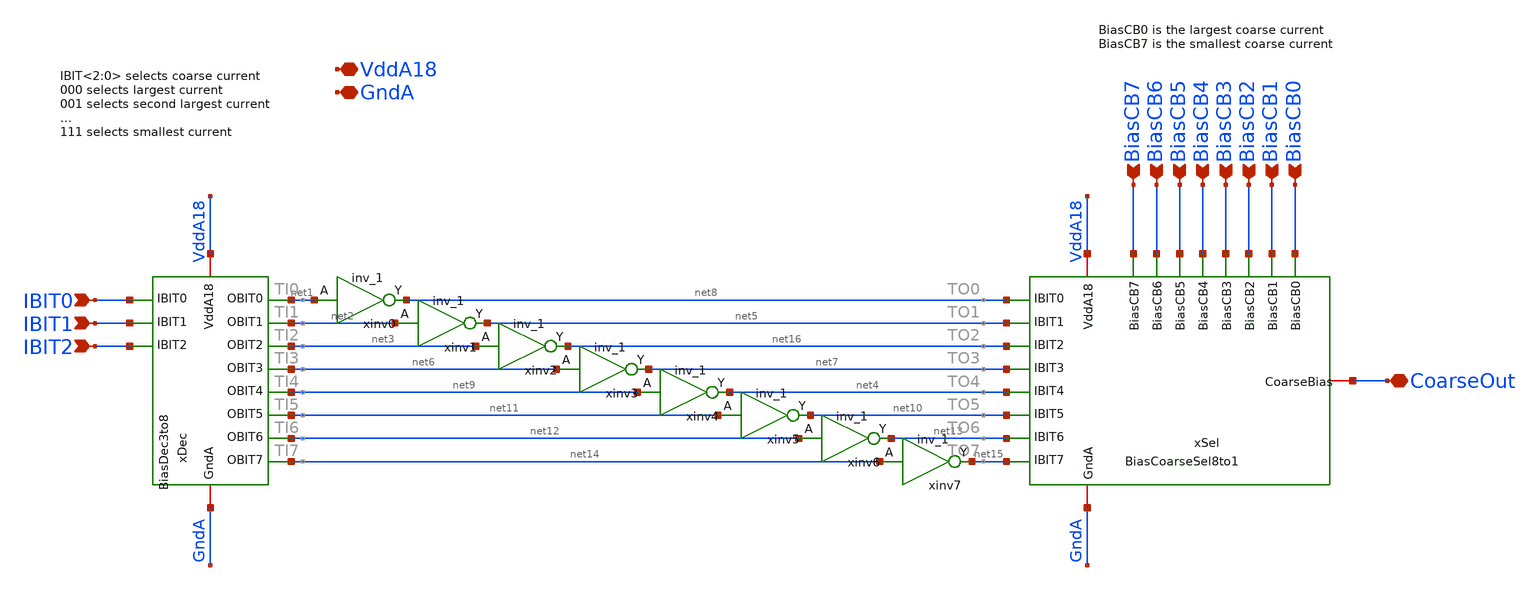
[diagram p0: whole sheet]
** sch_path: analog/xschem/BiasCoarseBuffer.sch
**.subckt BiasCoarseBuffer VddA18 GndA BiasCB7 BiasCB6 BiasCB5 BiasCB4 BiasCB3 BiasCB2 BiasCB1
*+ BiasCB0 IBIT0 IBIT1 IBIT2 CoarseOut
*.iopin VddA18
*.iopin GndA
*.ipin BiasCB7
*.ipin BiasCB6
*.ipin BiasCB5
*.ipin BiasCB4
*.ipin BiasCB3
*.ipin BiasCB2
*.ipin BiasCB1
*.ipin BiasCB0
*.ipin IBIT0
*.ipin IBIT1
*.ipin IBIT2
*.iopin CoarseOut
xSel VddA18 GndA net8 net5 net7 net4 net10 net13 net15 net16 BiasCB0 BiasCB1 BiasCB3 BiasCB4 BiasCB5
+ BiasCB6 BiasCB7 BiasCB2 CoarseOut BiasCoarseSel8to1
xDec VddA18 GndA net1 net2 net6 net9 net11 net12 net14 net3 IBIT0 IBIT1 IBIT2 BiasDec3to8
xinv0 net1 VGND VNB VPB VPWR net8 sky130_fd_sc_hd__inv_1
xinv1 net2 VGND VNB VPB VPWR net5 sky130_fd_sc_hd__inv_1
xinv2 net3 VGND VNB VPB VPWR net16 sky130_fd_sc_hd__inv_1
xinv3 net6 VGND VNB VPB VPWR net7 sky130_fd_sc_hd__inv_1
xinv4 net9 VGND VNB VPB VPWR net4 sky130_fd_sc_hd__inv_1
xinv5 net11 VGND VNB VPB VPWR net10 sky130_fd_sc_hd__inv_1
xinv6 net12 VGND VNB VPB VPWR net13 sky130_fd_sc_hd__inv_1
xinv7 net14 VGND VNB VPB VPWR net15 sky130_fd_sc_hd__inv_1
**.ends
.end
